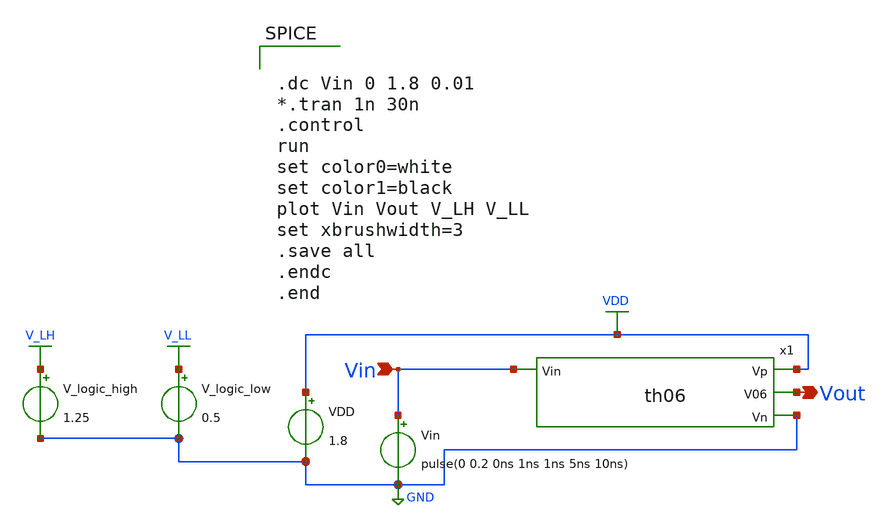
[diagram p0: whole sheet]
** sch_path: xschem/Vth_sch/Pre_layout/th06.sch
**.subckt th06 Vin Vout
*.ipin Vin
*.opin Vout
VDD VDD GND 1.8
Vin Vin GND pulse(0 0.2 0ns 1ns 1ns 5ns 10ns)
V_logic_high V_LH GND 1.25
V_logic_low V_LL GND 0.5
x1 VDD Vin Vout GND th06
**** begin user architecture code


.lib /usr/local/share/pdk/sky130A/libs.tech/ngspice/sky130.lib.spice tt

.save all





.dc Vin 0 1.8 0.01
*.tran 1n 30n
.control
run
set color0=white
set color1=black
plot Vin Vout V_LH V_LL
set xbrushwidth=3
.save all
.endc
.end


**** end user architecture code
**.ends

* expanding   symbol:  /home/exotic/Desktop/ASIC_ADC/xschem/Vth_sch/Symbol/th06.sym # of pins=4
** sym_path: xschem/Vth_sch/Symbol/th06.sym
** sch_path: xschem/Vth_sch/Symbol/th06.sch
.subckt th06 Vp Vin V06 Vn
*.opin Vn
*.opin Vp
*.ipin Vin
*.opin V06
XM2 V06 net1 Vp Vp sky130_fd_pr__pfet_01v8 L=0.436 W=0.422 nf=1 ad='int((nf+1)/2) * W/nf * 0.29' as='int((nf+2)/2) * W/nf * 0.29'
+ pd='2*int((nf+1)/2) * (W/nf + 0.29)' ps='2*int((nf+2)/2) * (W/nf + 0.29)' nrd='0.29 / W' nrs='0.29 / W'
+ sa=0 sb=0 sd=0 mult=1 m=1
XM3 V06 net1 Vn Vn sky130_fd_pr__nfet_01v8 L=0.15 W=0.462 nf=1 ad='int((nf+1)/2) * W/nf * 0.29' as='int((nf+2)/2) * W/nf * 0.29'
+ pd='2*int((nf+1)/2) * (W/nf + 0.29)' ps='2*int((nf+2)/2) * (W/nf + 0.29)' nrd='0.29 / W' nrs='0.29 / W'
+ sa=0 sb=0 sd=0 mult=1 m=1
XM1 net1 Vin Vp Vp sky130_fd_pr__pfet_01v8 L=0.494 W=0.42 nf=1 ad='int((nf+1)/2) * W/nf * 0.29' as='int((nf+2)/2) * W/nf * 0.29'
+ pd='2*int((nf+1)/2) * (W/nf + 0.29)' ps='2*int((nf+2)/2) * (W/nf + 0.29)' nrd='0.29 / W' nrs='0.29 / W'
+ sa=0 sb=0 sd=0 mult=1 m=1
XM0 net1 Vin Vn Vn sky130_fd_pr__nfet_01v8 L=0.152 W=0.393 nf=1 ad='int((nf+1)/2) * W/nf * 0.29' as='int((nf+2)/2) * W/nf * 0.29'
+ pd='2*int((nf+1)/2) * (W/nf + 0.29)' ps='2*int((nf+2)/2) * (W/nf + 0.29)' nrd='0.29 / W' nrs='0.29 / W'
+ sa=0 sb=0 sd=0 mult=1 m=1
.ends

.GLOBAL VDD
.GLOBAL GND
.GLOBAL V_LH
.GLOBAL V_LL
.end
